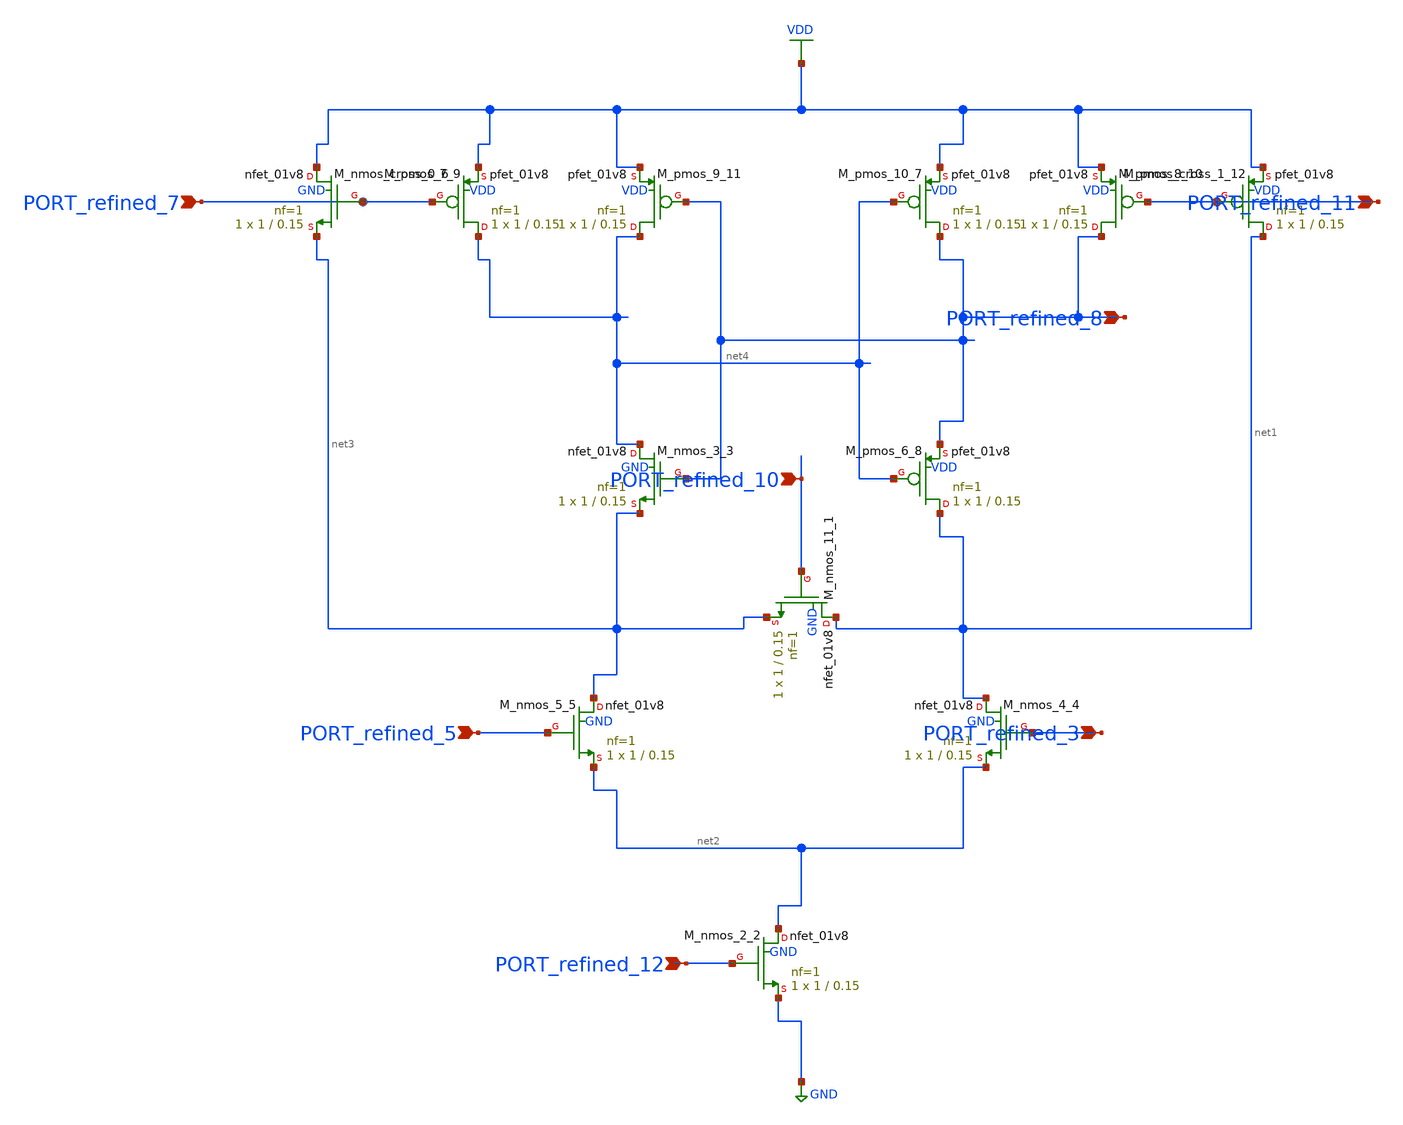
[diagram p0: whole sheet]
** sch_path: schematics/Image2Net/123.sch
**.subckt 123 PORT_refined_12 PORT_refined_3 PORT_refined_5 PORT_refined_11 PORT_refined_8
*+ PORT_refined_7 PORT_refined_10
*.ipin PORT_refined_12
*.ipin PORT_refined_3
*.ipin PORT_refined_5
*.ipin PORT_refined_11
*.ipin PORT_refined_8
*.ipin PORT_refined_7
*.ipin PORT_refined_10
XM_nmos_11_1 net1 PORT_refined_10 net3 GND sky130_fd_pr__nfet_01v8 L=0.15 W=1 nf=1 ad='int((1 + 1)/2) * 1 / 1 * 0.29'
+ as='int((1 + 2)/2) * 1 / 1 * 0.29' pd='2*int((1 + 1)/2) * (1 / 1 + 0.29)' ps='2*int((1 + 2)/2) * (1 / 1 + 0.29)'
+ nrd='0.29 / 1 ' nrs='0.29 / 1 ' sa=0 sb=0 sd=0 mult=1 m=1
XM_nmos_2_2 net2 PORT_refined_12 GND GND sky130_fd_pr__nfet_01v8 L=0.15 W=1 nf=1 ad='int((1 + 1)/2) * 1 / 1 * 0.29'
+ as='int((1 + 2)/2) * 1 / 1 * 0.29' pd='2*int((1 + 1)/2) * (1 / 1 + 0.29)' ps='2*int((1 + 2)/2) * (1 / 1 + 0.29)'
+ nrd='0.29 / 1 ' nrs='0.29 / 1 ' sa=0 sb=0 sd=0 mult=1 m=1
XM_nmos_3_3 net4 PORT_refined_8 net3 GND sky130_fd_pr__nfet_01v8 L=0.15 W=1 nf=1 ad='int((1 + 1)/2) * 1 / 1 * 0.29'
+ as='int((1 + 2)/2) * 1 / 1 * 0.29' pd='2*int((1 + 1)/2) * (1 / 1 + 0.29)' ps='2*int((1 + 2)/2) * (1 / 1 + 0.29)'
+ nrd='0.29 / 1 ' nrs='0.29 / 1 ' sa=0 sb=0 sd=0 mult=1 m=1
XM_nmos_4_4 net1 PORT_refined_3 net2 GND sky130_fd_pr__nfet_01v8 L=0.15 W=1 nf=1 ad='int((1 + 1)/2) * 1 / 1 * 0.29'
+ as='int((1 + 2)/2) * 1 / 1 * 0.29' pd='2*int((1 + 1)/2) * (1 / 1 + 0.29)' ps='2*int((1 + 2)/2) * (1 / 1 + 0.29)'
+ nrd='0.29 / 1 ' nrs='0.29 / 1 ' sa=0 sb=0 sd=0 mult=1 m=1
XM_nmos_5_5 net3 PORT_refined_5 net2 GND sky130_fd_pr__nfet_01v8 L=0.15 W=1 nf=1 ad='int((1 + 1)/2) * 1 / 1 * 0.29'
+ as='int((1 + 2)/2) * 1 / 1 * 0.29' pd='2*int((1 + 1)/2) * (1 / 1 + 0.29)' ps='2*int((1 + 2)/2) * (1 / 1 + 0.29)'
+ nrd='0.29 / 1 ' nrs='0.29 / 1 ' sa=0 sb=0 sd=0 mult=1 m=1
XM_nmos_cross_0_6 VDD PORT_refined_7 net3 GND sky130_fd_pr__nfet_01v8 L=0.15 W=1 nf=1 ad='int((1 + 1)/2) * 1 / 1 * 0.29'
+ as='int((1 + 2)/2) * 1 / 1 * 0.29' pd='2*int((1 + 1)/2) * (1 / 1 + 0.29)' ps='2*int((1 + 2)/2) * (1 / 1 + 0.29)'
+ nrd='0.29 / 1 ' nrs='0.29 / 1 ' sa=0 sb=0 sd=0 mult=1 m=1
XM_pmos_10_7 PORT_refined_8 net4 VDD VDD sky130_fd_pr__pfet_01v8 L=0.15 W=1 nf=1 ad='int((1 + 1)/2) * 1 / 1 * 0.29'
+ as='int((1 + 2)/2) * 1 / 1 * 0.29' pd='2*int((1 + 1)/2) * (1 / 1 + 0.29)' ps='2*int((1 + 2)/2) * (1 / 1 + 0.29)'
+ nrd='0.29 / 1 ' nrs='0.29 / 1 ' sa=0 sb=0 sd=0 mult=1 m=1
XM_pmos_6_8 net1 net4 PORT_refined_8 VDD sky130_fd_pr__pfet_01v8 L=0.15 W=1 nf=1 ad='int((1 + 1)/2) * 1 / 1 * 0.29'
+ as='int((1 + 2)/2) * 1 / 1 * 0.29' pd='2*int((1 + 1)/2) * (1 / 1 + 0.29)' ps='2*int((1 + 2)/2) * (1 / 1 + 0.29)'
+ nrd='0.29 / 1 ' nrs='0.29 / 1 ' sa=0 sb=0 sd=0 mult=1 m=1
XM_pmos_7_9 net4 PORT_refined_7 VDD VDD sky130_fd_pr__pfet_01v8 L=0.15 W=1 nf=1 ad='int((1 + 1)/2) * 1 / 1 * 0.29'
+ as='int((1 + 2)/2) * 1 / 1 * 0.29' pd='2*int((1 + 1)/2) * (1 / 1 + 0.29)' ps='2*int((1 + 2)/2) * (1 / 1 + 0.29)'
+ nrd='0.29 / 1 ' nrs='0.29 / 1 ' sa=0 sb=0 sd=0 mult=1 m=1
XM_pmos_8_10 PORT_refined_8 PORT_refined_11 VDD VDD sky130_fd_pr__pfet_01v8 L=0.15 W=1 nf=1 ad='int((1 + 1)/2) * 1 / 1 * 0.29'
+ as='int((1 + 2)/2) * 1 / 1 * 0.29' pd='2*int((1 + 1)/2) * (1 / 1 + 0.29)' ps='2*int((1 + 2)/2) * (1 / 1 + 0.29)'
+ nrd='0.29 / 1 ' nrs='0.29 / 1 ' sa=0 sb=0 sd=0 mult=1 m=1
XM_pmos_9_11 net4 PORT_refined_8 VDD VDD sky130_fd_pr__pfet_01v8 L=0.15 W=1 nf=1 ad='int((1 + 1)/2) * 1 / 1 * 0.29'
+ as='int((1 + 2)/2) * 1 / 1 * 0.29' pd='2*int((1 + 1)/2) * (1 / 1 + 0.29)' ps='2*int((1 + 2)/2) * (1 / 1 + 0.29)'
+ nrd='0.29 / 1 ' nrs='0.29 / 1 ' sa=0 sb=0 sd=0 mult=1 m=1
XM_pmos_cross_1_12 net1 PORT_refined_11 VDD VDD sky130_fd_pr__pfet_01v8 L=0.15 W=1 nf=1 ad='int((1 + 1)/2) * 1 / 1 * 0.29'
+ as='int((1 + 2)/2) * 1 / 1 * 0.29' pd='2*int((1 + 1)/2) * (1 / 1 + 0.29)' ps='2*int((1 + 2)/2) * (1 / 1 + 0.29)'
+ nrd='0.29 / 1 ' nrs='0.29 / 1 ' sa=0 sb=0 sd=0 mult=1 m=1
**.ends
.GLOBAL GND
.GLOBAL VDD
.end
